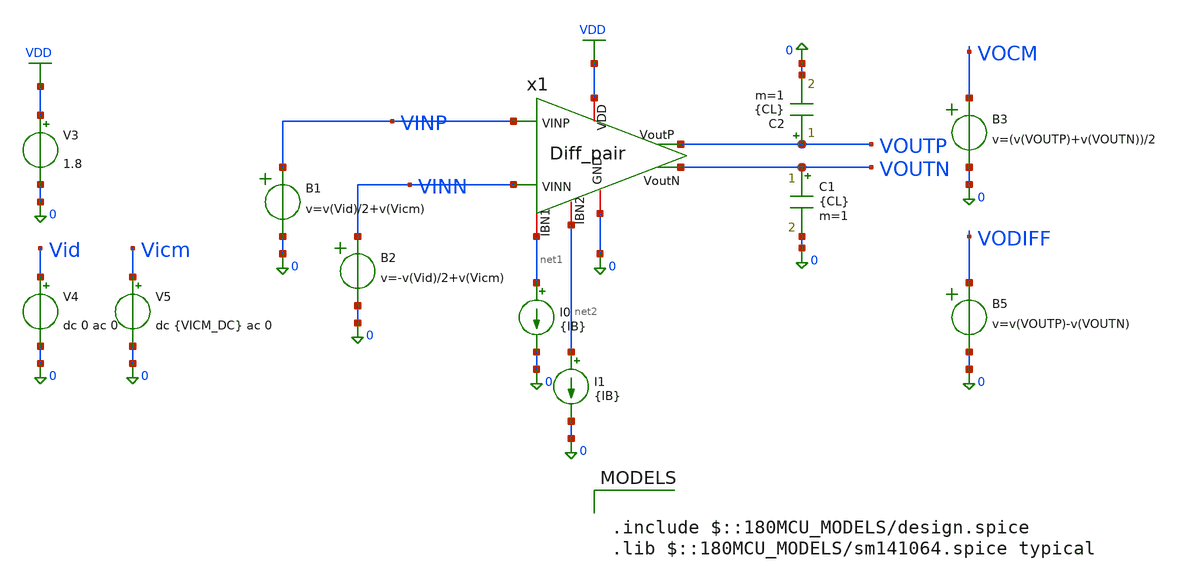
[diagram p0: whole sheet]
** sch_path: Lab_06/Diff_pair_TB.sch
**.subckt Diff_pair_TB
x1 0 VDD net1 VINP VINN VOUTP VOUTN net2 Diff_pair WP1=45.2u LP1=1.1u WP2=44u LP2=0.35u RD=27.5k
C1 VOUTN 0 {CL} m=1
C2 VOUTP 0 {CL} m=1
I0 net1 0 {IB}
V3 VDD 0 1.8
V4 Vid 0 dc 0 ac 0
V5 Vicm 0 dc {VICM_DC} ac 0
B1 VINP 0 v=v(Vid)/2+v(Vicm)
B2 VINN 0 v=-v(Vid)/2+v(Vicm)
B5 VODIFF 0 v=v(VOUTP)-v(VOUTN)
B3 VOCM 0 v=(v(VOUTP)+v(VOUTN))/2
I1 net2 0 {IB}
**** begin user architecture code


.param IB=20u CL=1p VICM_DC={1.8-0.5-0.94}
.control
alterparam sw_stat_global = 0
alterparam sw_stat_mismatch = 0
reset
save all

let x = 1
set num = {$&x}
dowhile x <= 7
save @m.x1.xm{$num}.m0[id]
save @m.x1.xm{$num}.m0[vgs]
save @m.x1.xm{$num}.m0[vds]
save @m.x1.xm{$num}.m0[vdsat]
save @m.x1.xm{$num}.m0[vth]
save @m.x1.xm{$num}.m0[gm]
save @m.x1.xm{$num}.m0[gds]
save @m.x1.xm{$num}.m0[gmbs]
save @m.x1.xm{$num}.m0[cgg]
save @m.x1.xm{$num}.m0[cdd]
save @m.x1.xm{$num}.m0[css]
let x = x + 1
set num = {$&x}
end

* === OP Point ===
op
write diff_amp_tb_op_ac.raw
set appendwrite
echo " === MOSFET Operating Points ==="
show m : id : vgs : vds : vth : vdsat : gm : gds : gmbs
echo " === Bias Points ==="
let x = 1
dowhile x <= 7
 set num = {$&x}
 let gmid = @m.x1.xm{$num}.m0[gm]/@m.x1.xm{$num}.m0[id]
 let Vstar = 2/gmid
 echo "M{$num}: gm/id = $&gmid S/A, Vstar = $&Vstar V"
 let x = x + 1
end

* === DIFFERENTIAL AC ===
alter V4 AC = 1
alter V5 AC = 0
ac dec 10 1 10e9

* === COMMON MODE AC ===
alter V4 AC = 0
alter V5 AC = 1
ac dec 10 1 10e9

* === EXTRACT RESULTS ===
set units=degrees
let vod = ac1.v(VODIFF)
let vocm = ac2.v(VOCM)
let CMRR = vdb(vod) - vdb(vocm)

* === MEASUREMENTS ===
meas ac Av_diff_db find vdb(vod) at=1
meas ac Av_diff_mag find vmag(vod) at=1
let A3db = Av_diff_mag/sqrt(2)
meas ac BW_diff when vmag(vod)=A3db fall=1

meas ac Av_CM_db find vdb(vocm) at=1
meas ac Av_CM_mag find vmag(vocm) at=1
let A3db_cm = Av_CM_mag/sqrt(2)
meas ac BW_CM when vmag(vocm)=A3db_cm fall=1

let CMRR_db = Av_diff_db - Av_CM_db

* === DISPLAY RESULTS ===
echo " === AC Results ==="
echo "Av Diff: $&Av_diff_db dB, BW: $&BW_diff Hz"
echo "Av CM: $&Av_CM_db dB, BW: $&BW_CM Hz"
echo "CMRR: $&CMRR_db dB"
write diff_amp_tb_op_ac.raw
.endc



.include $::180MCU_MODELS/design.spice
.lib $::180MCU_MODELS/sm141064.spice typical

**** end user architecture code
**.ends

* expanding   symbol:  Diff_pair.sym # of pins=8
** sym_path: Lab_06/Diff_pair.sym
** sch_path: Lab_06/Diff_pair.sch
.subckt Diff_pair GND VDD IBN1 VINP VINN VoutP VoutN IBN2  WP1=1u LP1=0.5u WP2=1u LP2=0.5u RD=1k
*.iopin IBN1
*.ipin VINP
*.opin VoutP
*.ipin VINN
*.iopin VDD
*.iopin GND
*.opin VoutN
*.iopin IBN2
XM1 VoutN VINP net1 VDD pfet_03v3 L={LP2} W={WP2} nf=1 ad='int((nf+1)/2) * W/nf * 0.18u' as='int((nf+2)/2) * W/nf * 0.18u'
+ pd='2*int((nf+1)/2) * (W/nf + 0.18u)' ps='2*int((nf+2)/2) * (W/nf + 0.18u)' nrd='0.18u / W' nrs='0.18u / W'
+ sa=0 sb=0 sd=0 m=1
XM2 VoutP VINN net1 VDD pfet_03v3 L={LP2} W={WP2} nf=1 ad='int((nf+1)/2) * W/nf * 0.18u' as='int((nf+2)/2) * W/nf * 0.18u'
+ pd='2*int((nf+1)/2) * (W/nf + 0.18u)' ps='2*int((nf+2)/2) * (W/nf + 0.18u)' nrd='0.18u / W' nrs='0.18u / W'
+ sa=0 sb=0 sd=0 m=1
XM3 net2 IBN2 VDD VDD pfet_03v3 L={LP1} W={WP1*2} nf=1 ad='int((nf+1)/2) * W/nf * 0.18u' as='int((nf+2)/2) * W/nf * 0.18u'
+ pd='2*int((nf+1)/2) * (W/nf + 0.18u)' ps='2*int((nf+2)/2) * (W/nf + 0.18u)' nrd='0.18u / W' nrs='0.18u / W'
+ sa=0 sb=0 sd=0 m=1
XM4 net3 IBN2 VDD VDD pfet_03v3 L={LP1} W={WP1} nf=1 ad='int((nf+1)/2) * W/nf * 0.18u' as='int((nf+2)/2) * W/nf * 0.18u'
+ pd='2*int((nf+1)/2) * (W/nf + 0.18u)' ps='2*int((nf+2)/2) * (W/nf + 0.18u)' nrd='0.18u / W' nrs='0.18u / W'
+ sa=0 sb=0 sd=0 m=1
R2 VoutP GND {RD} m=1
R1 VoutN GND {RD} m=1
XM5 IBN1 IBN1 VDD VDD pfet_03v3 L={LP1} W={WP1*0.25} nf=1 ad='int((nf+1)/2) * W/nf * 0.18u' as='int((nf+2)/2) * W/nf * 0.18u'
+ pd='2*int((nf+1)/2) * (W/nf + 0.18u)' ps='2*int((nf+2)/2) * (W/nf + 0.18u)' nrd='0.18u / W' nrs='0.18u / W'
+ sa=0 sb=0 sd=0 m=1
XM6 IBN2 IBN1 net3 net3 pfet_03v3 L={LP1} W={WP1} nf=1 ad='int((nf+1)/2) * W/nf * 0.18u' as='int((nf+2)/2) * W/nf * 0.18u'
+ pd='2*int((nf+1)/2) * (W/nf + 0.18u)' ps='2*int((nf+2)/2) * (W/nf + 0.18u)' nrd='0.18u / W' nrs='0.18u / W'
+ sa=0 sb=0 sd=0 m=1
XM7 net1 IBN1 net2 net2 pfet_03v3 L={LP1} W={WP1*2} nf=1 ad='int((nf+1)/2) * W/nf * 0.18u' as='int((nf+2)/2) * W/nf * 0.18u'
+ pd='2*int((nf+1)/2) * (W/nf + 0.18u)' ps='2*int((nf+2)/2) * (W/nf + 0.18u)' nrd='0.18u / W' nrs='0.18u / W'
+ sa=0 sb=0 sd=0 m=1
.ends

.GLOBAL VDD
.end
